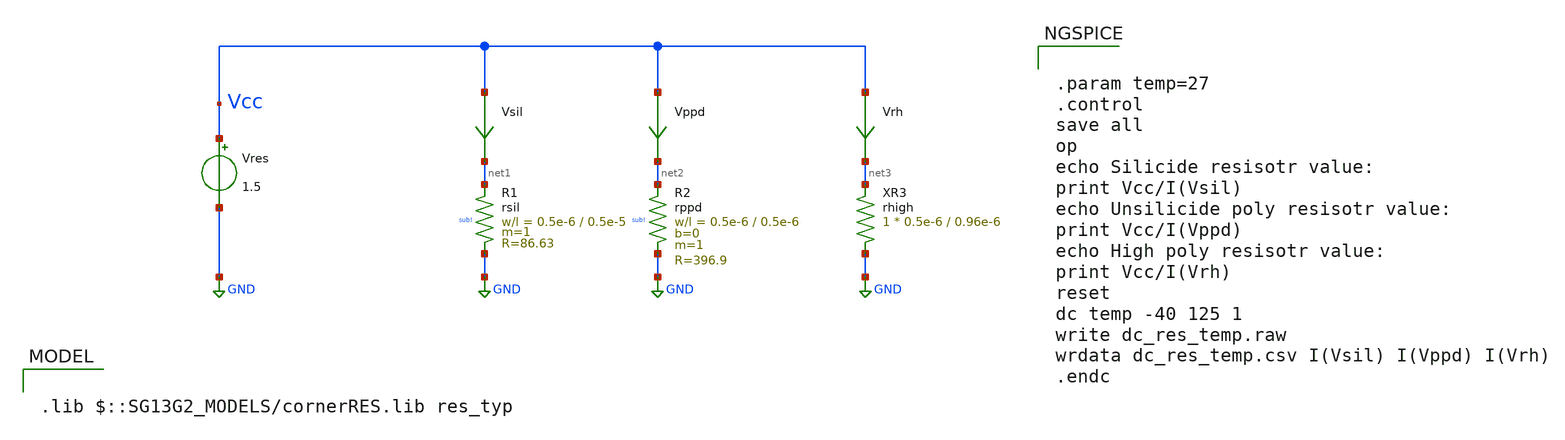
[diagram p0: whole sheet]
** sch_path: ihp-sg13g2/libs.tech/xschem/sg13g2_tests/dc_res_temp.sch
* Copyright 2023 IHP PDK Authors
**.subckt dc_res_temp
Vres Vcc GND 1.5
Vsil Vcc net1 0
.save i(vsil)
Vppd Vcc net2 0
.save i(vppd)
Vrh Vcc net3 0
.save i(vrh)
XR1 net1 GND sub! rsil w=0.5e-6 l=0.5e-5 m=1 mm_ok=1
XR2 net2 GND sub! rppd w=0.5e-6 l=0.5e-6 m=1 b=0 mm_ok=1
XR3 GND net3 rhigh w=0.5e-6 l=0.96e-6 m=1 R=1360.0 Imax=0.3e-6
**** begin user architecture code

.lib $::SG13G2_MODELS/cornerRES.lib res_typ



.param temp=27
.control
save all
op
echo Silicide resisotr value:
print Vcc/I(Vsil)
echo Unsilicide poly resisotr value:
print Vcc/I(Vppd)
echo High poly resisotr value:
print Vcc/I(Vrh)
reset
dc temp -40 125 1
write dc_res_temp.raw
wrdata dc_res_temp.csv I(Vsil) I(Vppd) I(Vrh)
.endc


**** end user architecture code
**.ends
.GLOBAL GND
.end
